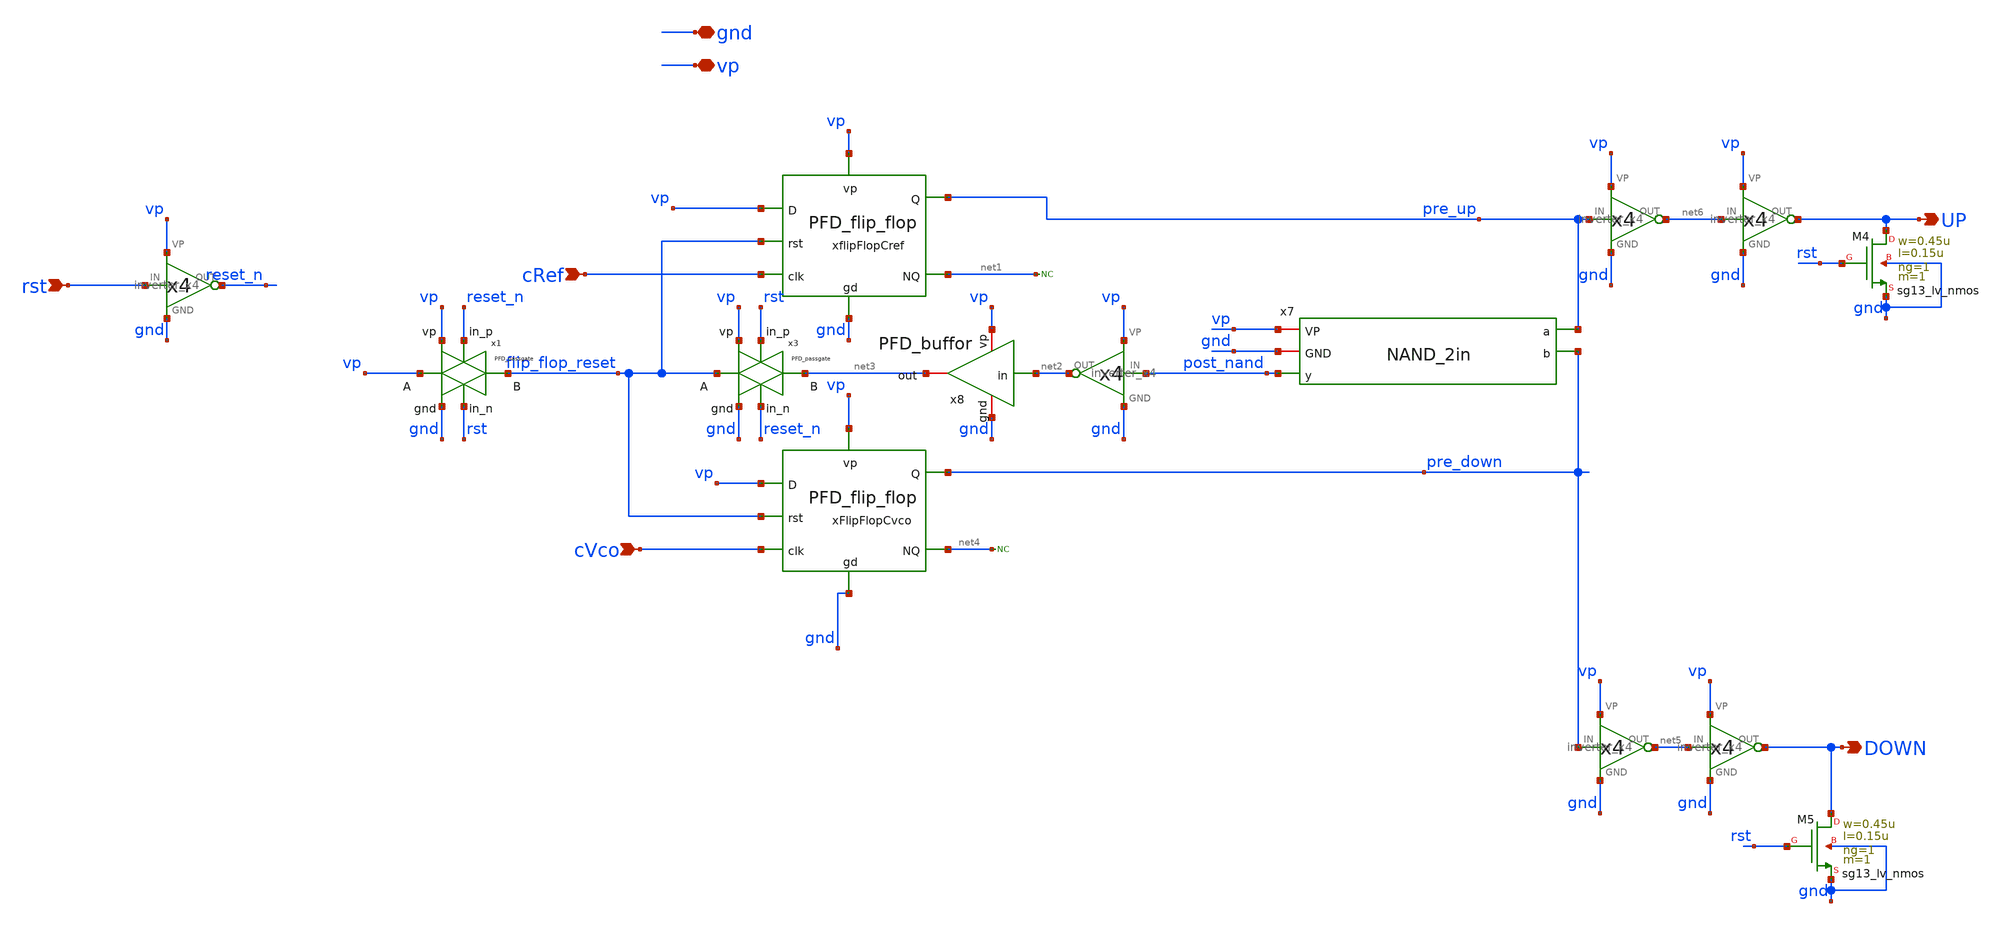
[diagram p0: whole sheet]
** sch_path: schematics/PFD/PFD_cell_2.sch
**.subckt PFD_cell_2 gnd vp cRef cVco rst UP DOWN
*.iopin gnd
*.iopin vp
*.ipin cRef
*.ipin cVco
*.ipin rst
*.opin UP
*.opin DOWN
x7 vp gnd pre_up post_nand pre_down NAND_2in
* noconn #net1
* noconn #net4
x9 rst reset_n vp gnd inverter_x4
xflipFlopCref cRef flip_flop_reset vp pre_up net1 vp gnd PFD_flip_flop
xFlipFlopCvco cVco flip_flop_reset vp pre_down net4 vp gnd PFD_flip_flop
XM4 UP rst gnd gnd sg13_lv_nmos w=0.45u l=0.15u ng=1 m=1 mm_ok=1
XM5 DOWN rst gnd gnd sg13_lv_nmos w=0.45u l=0.15u ng=1 m=1 mm_ok=1
x4 net6 UP vp gnd inverter_x4
x6 net5 DOWN vp gnd inverter_x4
x2 pre_up net6 vp gnd inverter_x4
x5 pre_down net5 vp gnd inverter_x4
x1 rst vp vp flip_flop_reset gnd reset_n PFD_passgate
x3 reset_n vp flip_flop_reset net3 gnd rst PFD_passgate
x8 gnd vp net3 net2 PFD_buffor
x11 post_nand net2 vp gnd inverter_x4
**.ends
.end
